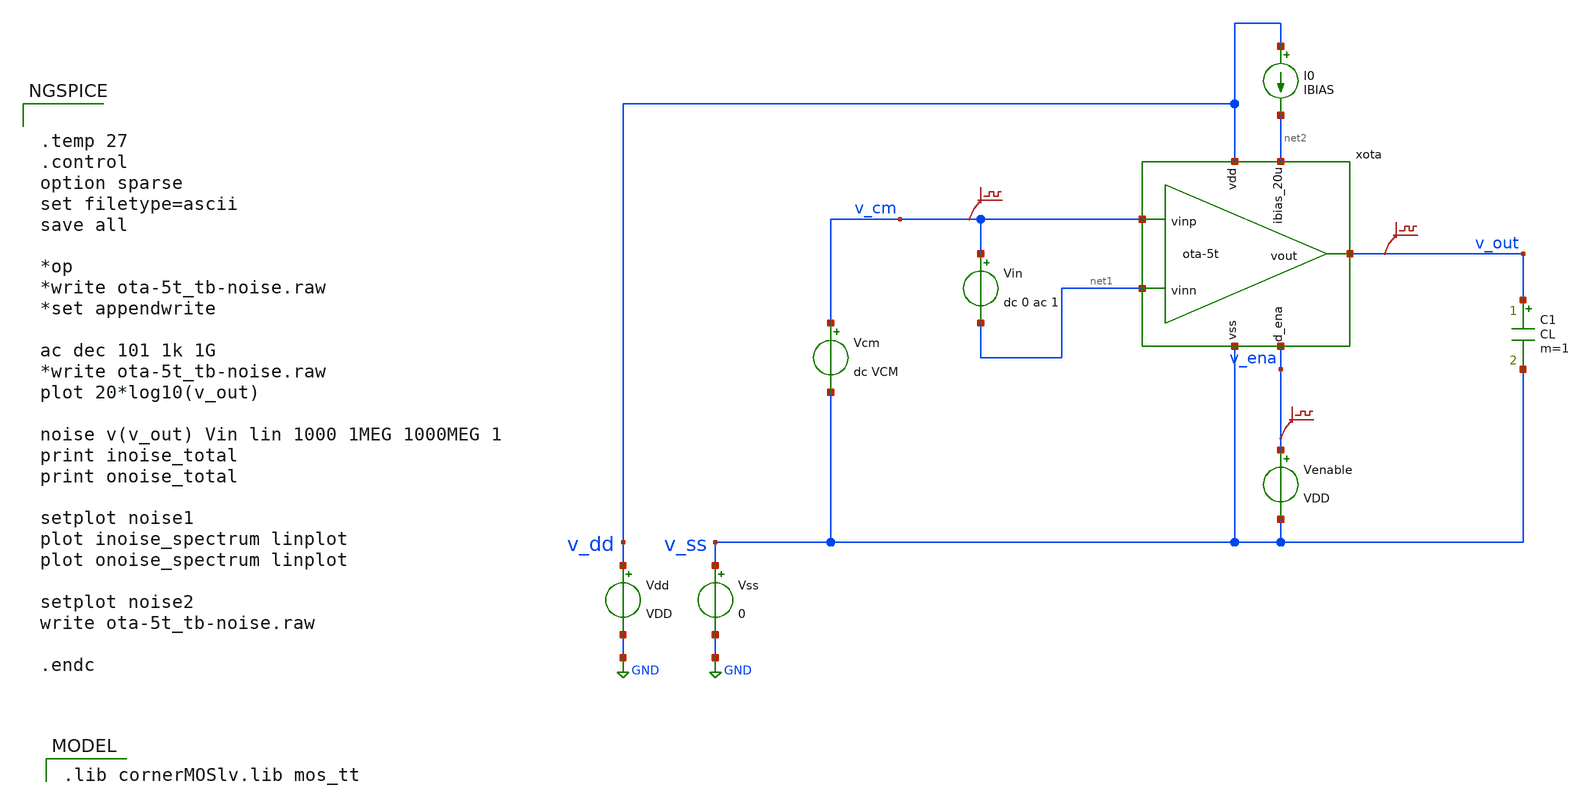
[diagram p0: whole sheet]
** sch_path: platform/examples/OTA/5t-ota/ihp-sg13g2/xschem/ota-5t_tb-noise.sch
* (c) 2024-2025 H. Pretl, Apache-2.0 license
**.subckt ota-5t_tb-noise
Vdd v_dd GND VDD
xota v_dd v_out v_cm net1 net2 v_ena v_ss ota-5t
Vss v_ss GND 0
C1 v_out v_ss CL m=1
Vcm v_cm v_ss dc VCM
I0 v_dd net2 IBIAS
Venable v_ena v_ss VDD
.save v(v_cm)
.save v(v_out)
.save v(v_ena)
Vin v_cm net1 dc 0 ac 1
**** begin user architecture code
 .lib cornerMOSlv.lib mos_tt



.temp 27
.control
option sparse
set filetype=ascii
save all

*op
*write ota-5t_tb-noise.raw
*set appendwrite

ac dec 101 1k 1G
*write ota-5t_tb-noise.raw
plot 20*log10(v_out)

noise v(v_out) Vin lin 1000 1MEG 1000MEG 1
print inoise_total
print onoise_total

setplot noise1
plot inoise_spectrum linplot
plot onoise_spectrum linplot

setplot noise2
write ota-5t_tb-noise.raw

.endc





.param VDD=1.5
.param VCM=0.8
.param CL=50f

.param IBIAS=20u

.param x_dut_nfet_input_w=0.5u
.param x_dut_nfet_input_l=5.0u

.param x_dut_nfet_mirror_w=2.0u
.param x_dut_nfet_mirror_l=5.0u

.param x_dut_pfet_load_w=1.5u
.param x_dut_pfet_load_l=5.0u

.param x_dut_nfet_mirror_ref_w=2.0u
.param x_dut_nfet_mirror_ref_l=5.0u



**** end user architecture code
**.ends

* expanding   symbol:  ota-5t.sym # of pins=7
** sym_path: ota-5t.sym
** sch_path: ota-5t.sch
.subckt ota-5t vdd vout vinp vinn ibias_20u d_ena vss
*.ipin ibias_20u
*.iopin vdd
*.iopin vss
*.ipin vinp
*.ipin vinn
*.opin vout
*.ipin d_ena
XM5 tail gate_n vss vss sg13_lv_nmos w=x_dut_nfet_mirror_w l=x_dut_nfet_mirror_l ng=1 m=1 mm_ok=1
XM4 vout gate_p vdd vdd sg13_lv_pmos w=x_dut_pfet_load_w l=x_dut_pfet_load_l ng=1 m=1 mm_ok=1
XM1 gate_p vinp tail vss sg13_lv_nmos w=x_dut_nfet_input_w l=x_dut_nfet_input_l ng=1 m=1 mm_ok=1
XM2 vout vinn tail vss sg13_lv_nmos w=x_dut_nfet_input_w l=x_dut_nfet_input_l ng=1 m=1 mm_ok=1
XM3 gate_p gate_p vdd vdd sg13_lv_pmos w=x_dut_pfet_load_w l=x_dut_pfet_load_l ng=1 m=1 mm_ok=1
XM6 ibias_20u gate_n vss vss sg13_lv_nmos w=x_dut_nfet_mirror_ref_w l=x_dut_nfet_mirror_ref_l ng=1
+ m=1 mm_ok=1
XM9 gate_n ena_n vss vss sg13_lv_nmos w=0.5u l=0.13u ng=1 m=1 mm_ok=1
XM11 gate_p ena vdd vdd sg13_lv_pmos w=1.5u l=0.13u ng=1 m=1 mm_ok=1
XM7 ena ena_n vss vss sg13_lv_nmos w=0.5u l=0.13u ng=1 m=1 mm_ok=1
XM8 ena ena_n vdd vdd sg13_lv_pmos w=1.5u l=0.13u ng=1 m=1 mm_ok=1
XM10 ibias_20u ena gate_n vss sg13_lv_nmos w=0.5u l=0.13u ng=1 m=1 mm_ok=1
XM12 ena_n d_ena vss vss sg13_lv_nmos w=0.5u l=0.13u ng=1 m=1 mm_ok=1
XM13 ena_n d_ena vdd vdd sg13_lv_pmos w=1.5u l=0.13u ng=1 m=1 mm_ok=1
.ends

.GLOBAL GND
.end
